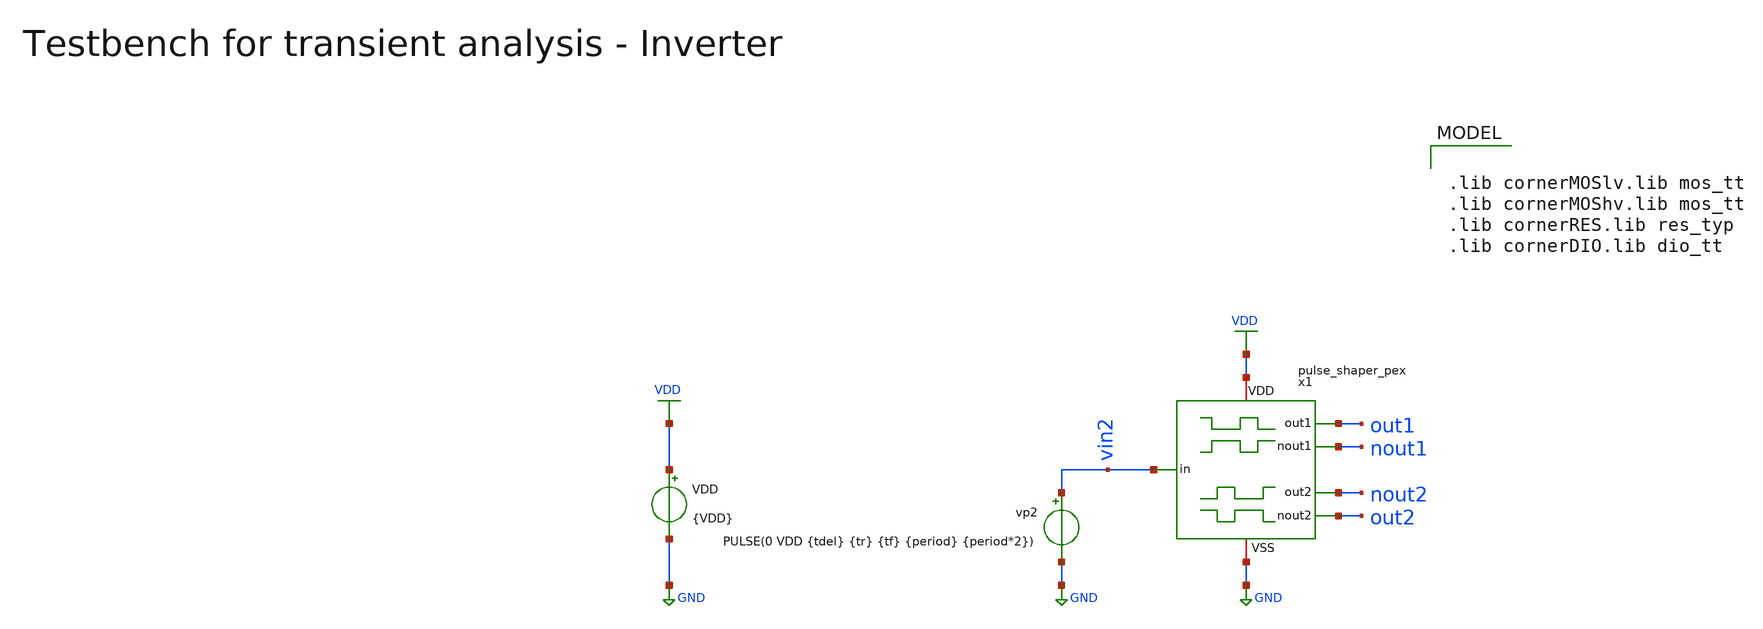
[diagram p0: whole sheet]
** sch_path: macros/heichips26_vcr/macros/switched_capacitor/testbenches/xschem/tb_pulse_shaper_pex_tran.sch
**.subckt tb_pulse_shaper_pex_tran
VDD VDD GND {VDD}
vp2 vin2 GND PULSE(0 VDD {tdel} {tr} {tf} {period} {period*2})
x1 out1 nout1 VDD vin2 GND nout2 out2 pulse_shaper_pex
**** begin user architecture code


.include ../../../netlist/pex/pulse_shaper_magic_pex_3.spice

.param VDD=3.3
.csparam VDD=VDD
.param Vcm=VDD/2
.param temp=27
.param Cload=10p
.param Rload=1k

.param period = 4n
.param tdel   = {period/2}
.param ton    = {period*2}
.csparam tstop  = {2.5*period}
.csparam tstep  = {period/100}
.param tr     = {period/100}
.param tf     = {period/100}

.options savecurrents klu method=gear reltol=1e-4 abstol=1e-15 gmin=1e-15
.control

save all

* Transient Analysis
tran {$&tstep} {$&tstop}
write @schname\.raw

* Plotting
plot vin2
plot out1+4 out2+4 nout1 nout2


*quit
.endc



.lib cornerMOSlv.lib mos_tt
.lib cornerMOShv.lib mos_tt
.lib cornerRES.lib res_typ
.lib cornerDIO.lib dio_tt

**** end user architecture code
**.ends
.GLOBAL GND
.GLOBAL VDD
.end
